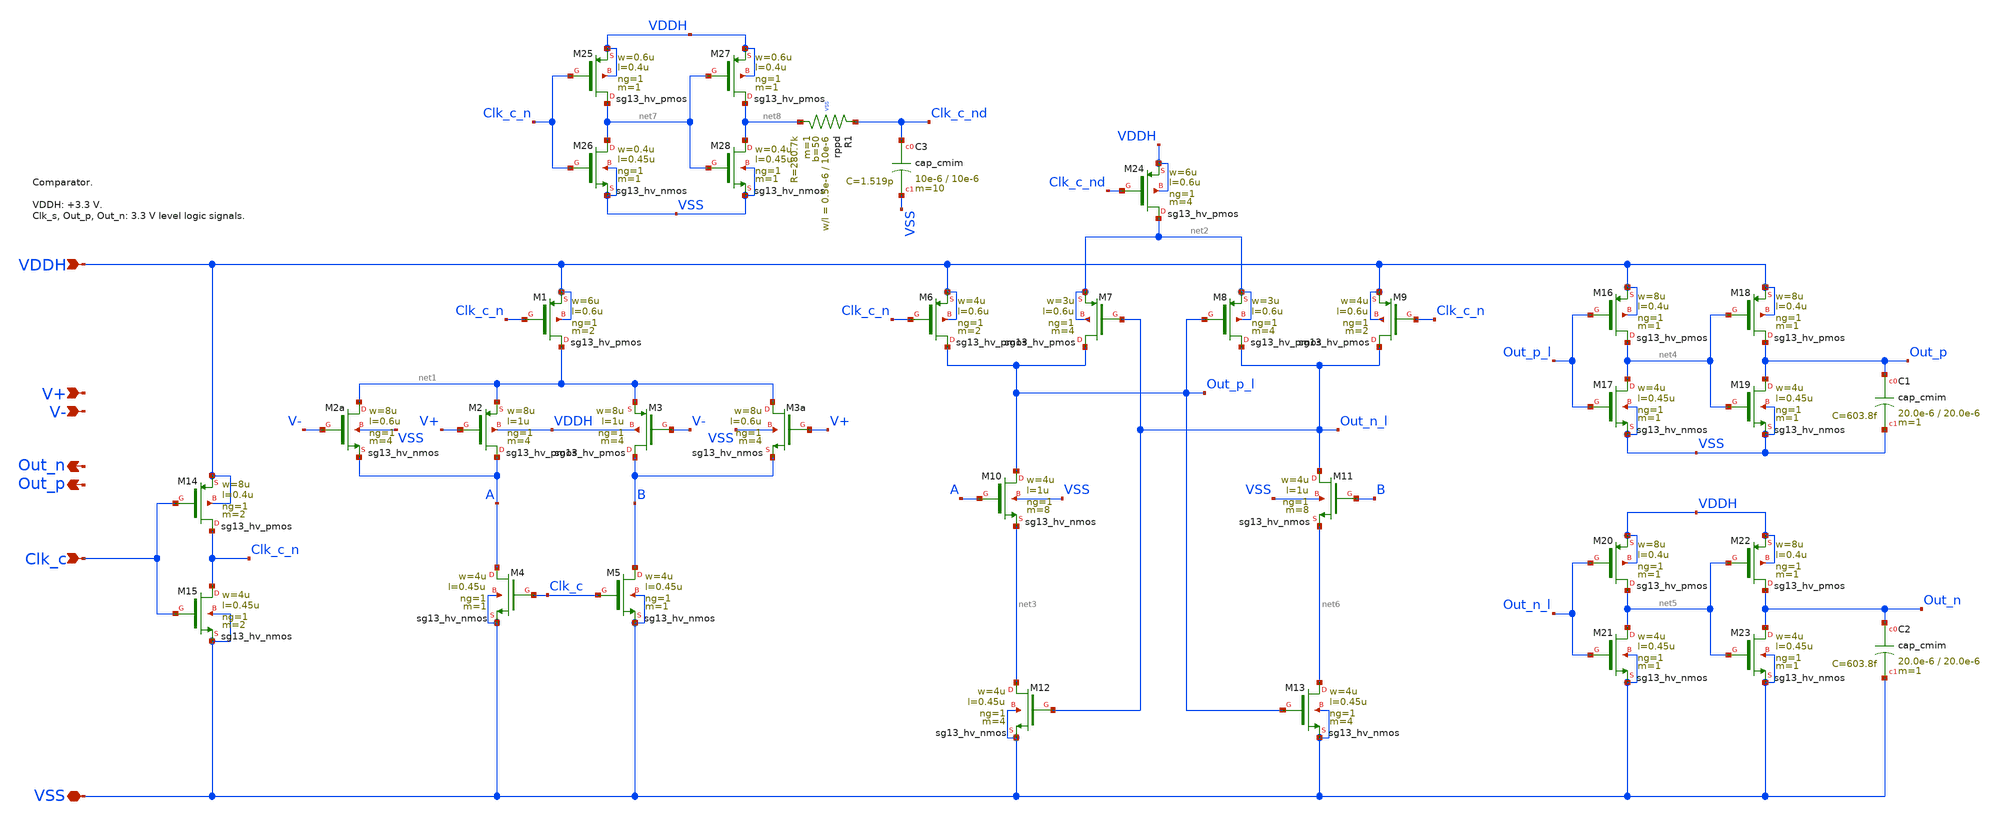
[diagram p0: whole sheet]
** sch_path: sar_adc/xschem/blocks/comparator/comparator_hv.sch
**.subckt comparator_hv Clk_c VSS VDDH V+ V- Out_p Out_n
*.ipin Clk_c
*.iopin VSS
*.ipin VDDH
*.ipin V+
*.ipin V-
*.opin Out_p
*.opin Out_n
XM14 Clk_c_n Clk_c VDDH VDDH sg13_hv_pmos w=8u l=0.4u ng=1 m=2 mm_ok=1
XM15 Clk_c_n Clk_c VSS VSS sg13_hv_nmos w=4u l=0.45u ng=1 m=2 mm_ok=1
XM1 net1 Clk_c_n VDDH VDDH sg13_hv_pmos w=6u l=0.6u ng=1 m=2 mm_ok=1
XM2 A V+ net1 VDDH sg13_hv_pmos w=8u l=1u ng=1 m=4 mm_ok=1
XM3 B V- net1 VDDH sg13_hv_pmos w=8u l=1u ng=1 m=4 mm_ok=1
XM2a net1 V- A VSS sg13_hv_nmos w=8u l=0.6u ng=1 m=4 mm_ok=1
XM3a net1 V+ B VSS sg13_hv_nmos w=8u l=0.6u ng=1 m=4 mm_ok=1
XM4 A Clk_c VSS VSS sg13_hv_nmos w=4u l=0.45u ng=1 m=1 mm_ok=1
XM5 B Clk_c VSS VSS sg13_hv_nmos w=4u l=0.45u ng=1 m=1 mm_ok=1
XM6 Out_p_l Clk_c_n VDDH VDDH sg13_hv_pmos w=4u l=0.6u ng=1 m=2 mm_ok=1
XM7 Out_p_l Out_n_l net2 net2 sg13_hv_pmos w=3u l=0.6u ng=1 m=4 mm_ok=1
XM8 Out_n_l Out_p_l net2 net2 sg13_hv_pmos w=3u l=0.6u ng=1 m=4 mm_ok=1
XM9 Out_n_l Clk_c_n VDDH VDDH sg13_hv_pmos w=4u l=0.6u ng=1 m=2 mm_ok=1
XM10 Out_p_l A net3 VSS sg13_hv_nmos w=4u l=1u ng=1 m=8 mm_ok=1
XM11 Out_n_l B net6 VSS sg13_hv_nmos w=4u l=1u ng=1 m=8 mm_ok=1
XM12 net3 Out_n_l VSS VSS sg13_hv_nmos w=4u l=0.45u ng=1 m=4 mm_ok=1
XM13 net6 Out_p_l VSS VSS sg13_hv_nmos w=4u l=0.45u ng=1 m=4 mm_ok=1
XM16 net4 Out_p_l VDDH VDDH sg13_hv_pmos w=8u l=0.4u ng=1 m=1 mm_ok=1
XM17 net4 Out_p_l VSS VSS sg13_hv_nmos w=4u l=0.45u ng=1 m=1 mm_ok=1
XM18 Out_p net4 VDDH VDDH sg13_hv_pmos w=8u l=0.4u ng=1 m=1 mm_ok=1
XM19 Out_p net4 VSS VSS sg13_hv_nmos w=4u l=0.45u ng=1 m=1 mm_ok=1
XM20 net5 Out_n_l VDDH VDDH sg13_hv_pmos w=8u l=0.4u ng=1 m=1 mm_ok=1
XM21 net5 Out_n_l VSS VSS sg13_hv_nmos w=4u l=0.45u ng=1 m=1 mm_ok=1
XM22 Out_n net5 VDDH VDDH sg13_hv_pmos w=8u l=0.4u ng=1 m=1 mm_ok=1
XM23 Out_n net5 VSS VSS sg13_hv_nmos w=4u l=0.45u ng=1 m=1 mm_ok=1
XC1 Out_p VSS cap_cmim w=20.0e-6 l=20.0e-6 m=1 mm_ok=1
XC2 Out_n VSS cap_cmim w=20.0e-6 l=20.0e-6 m=1 mm_ok=1
XM24 net2 Clk_c_nd VDDH VDDH sg13_hv_pmos w=6u l=0.6u ng=1 m=4 mm_ok=1
XM25 net7 Clk_c_n VDDH VDDH sg13_hv_pmos w=0.6u l=0.4u ng=1 m=1 mm_ok=1
XM26 net7 Clk_c_n VSS VSS sg13_hv_nmos w=0.4u l=0.45u ng=1 m=1 mm_ok=1
XM27 net8 net7 VDDH VDDH sg13_hv_pmos w=0.6u l=0.4u ng=1 m=1 mm_ok=1
XM28 net8 net7 VSS VSS sg13_hv_nmos w=0.4u l=0.45u ng=1 m=1 mm_ok=1
XR1 Clk_c_nd net8 VSS rppd w=0.5e-6 l=10e-6 m=1 b=50 mm_ok=1
XC3 Clk_c_nd VSS cap_cmim w=10e-6 l=10e-6 m=10 mm_ok=1
**.ends
.end
